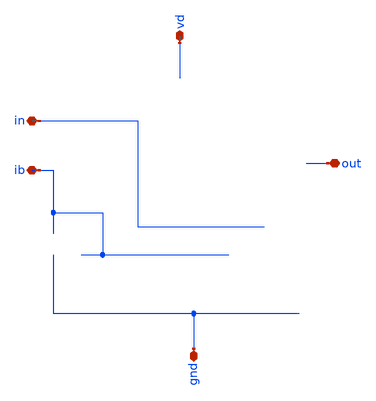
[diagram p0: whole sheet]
** sch_path: buffer/xschem/buffer-pex.sch
* Copyright 2020 Stefan Frederik Schippers
* Licensed under the Apache License, Version 2.0 (the "License");
* you may not use this file except in compliance with the License.
* You may obtain a copy of the License at
* https://www.apache.org/licenses/LICENSE-2.0
* Unless required by applicable law or agreed to in writing, software
* distributed under the License is distributed on an "AS IS" BASIS,
* WITHOUT WARRANTIES OR CONDITIONS OF ANY KIND, either express or implied.
* See the License for the specific language governing permissions and
* limitations under the License.
**.subckt buffer-pex vd ib out in gnd
*.iopin vd
*.iopin ib
*.iopin out
*.iopin in
*.iopin gnd
**** begin user architecture code


* NGSPICE file created from buffer.ext - technology: sky130A

*.subckt buffer vd ib out in gnd
X0 b.t2 b.t1 vd.t23 vd.t22 sky130_fd_pr__pfet_01v8 ad=0.145 pd=1.29 as=0.145 ps=1.29 w=1 l=1
X1 vd.t6 vd.t3 vd.t5 vd.t4 sky130_fd_pr__pfet_01v8 ad=0.29 pd=2.58 as=0 ps=0 w=1 l=1
X2 c out.t9 a gnd.t8 sky130_fd_pr__nfet_01v8 ad=0.248 pd=1.83 as=0.248 ps=1.83 w=1.5 l=0.15
X3 out.t5 d.t12 gnd.t19 gnd.t18 sky130_fd_pr__nfet_01v8 ad=0.725 pd=5.29 as=0.725 ps=5.29 w=5 l=1
X4 a a a vd.t39 sky130_fd_pr__pfet_01v8 ad=0.145 pd=1.29 as=1.16 ps=10.3 w=1 l=1
X5 d.t11 a vd.t38 vd.t37 sky130_fd_pr__pfet_01v8 ad=2.17 pd=15.3 as=2.17 ps=15.3 w=15 l=1
X6 d.t9 d.t8 d.t9 vd.t24 sky130_fd_pr__pfet_01v8 ad=2.17 pd=15.3 as=0 ps=0 w=15 l=1
X7 vd.t2 vd.t0 vd.t2 vd.t1 sky130_fd_pr__pfet_01v8 ad=0.145 pd=1.29 as=0 ps=0 w=1 l=1
X8 a a vd.t36 vd.t35 sky130_fd_pr__pfet_01v8 ad=0.145 pd=1.29 as=0.145 ps=1.29 w=1 l=1
X9 gnd.t22 d.t13 out.t8 gnd.t21 sky130_fd_pr__nfet_01v8 ad=0.725 pd=5.29 as=0.725 ps=5.29 w=5 l=1
X10 vd.t21 b.t16 out.t7 vd.t20 sky130_fd_pr__pfet_01v8 ad=2.17 pd=15.3 as=2.17 ps=15.3 w=15 l=1
X11 out.t4 out.t2 out.t3 vd.t40 sky130_fd_pr__pfet_01v8 ad=4.35 pd=30.6 as=0 ps=0 w=15 l=1
X12 d.t4 d.t3 gnd.t12 gnd.t11 sky130_fd_pr__nfet_01v8 ad=0.725 pd=5.29 as=0.725 ps=5.29 w=5 l=1
X13 a a vd.t34 vd.t33 sky130_fd_pr__pfet_01v8 ad=0.145 pd=1.29 as=0.145 ps=1.29 w=1 l=1
X14 b.t9 b.t7 b.t8 vd.t19 sky130_fd_pr__pfet_01v8 ad=0.29 pd=2.58 as=0 ps=0 w=1 l=1
X15 a a a gnd.t23 sky130_fd_pr__nfet_01v8 ad=0.465 pd=3.62 as=0.96 ps=7.28 w=1.5 l=0.15
X16 gnd.t7 gnd.t4 gnd.t6 gnd.t5 sky130_fd_pr__nfet_01v8 ad=1.45 pd=10.6 as=0 ps=0 w=5 l=1
X17 vd.t32 a a vd.t31 sky130_fd_pr__pfet_01v8 ad=0.145 pd=1.29 as=0.145 ps=1.29 w=1 l=1
X18 vd.t30 a a vd.t29 sky130_fd_pr__pfet_01v8 ad=0.145 pd=1.29 as=0.145 ps=1.29 w=1 l=1
X19 a a vd.t28 vd.t27 sky130_fd_pr__pfet_01v8 ad=0.145 pd=1.29 as=0.145 ps=1.29 w=1 l=1
X20 out.t10 d.t0 sky130_fd_pr__cap_mim_m3_1 l=15 w=30
X21 b.t6 b.t5 b.t6 gnd.t20 sky130_fd_pr__nfet_01v8 ad=0.248 pd=1.83 as=0 ps=0 w=1.5 l=0.15
X22 gnd.t10 ib.t0 ib.t1 gnd.t9 sky130_fd_pr__nfet_01v8 ad=0.145 pd=1.29 as=0.145 ps=1.29 w=1 l=1
X23 c ib.t5 gnd.t16 gnd.t15 sky130_fd_pr__nfet_01v8 ad=0.145 pd=1.29 as=0.145 ps=1.29 w=1 l=1
X24 ib.t4 ib.t2 ib.t3 gnd.t17 sky130_fd_pr__nfet_01v8 ad=0.29 pd=2.58 as=0 ps=0 w=1 l=1
X25 out.t6 b.t17 vd.t18 vd.t17 sky130_fd_pr__pfet_01v8 ad=2.17 pd=15.3 as=2.17 ps=15.3 w=15 l=1
X26 b.t15 b.t14 vd.t16 vd.t15 sky130_fd_pr__pfet_01v8 ad=0.145 pd=1.29 as=0.145 ps=1.29 w=1 l=1
X27 vd.t14 b.t10 b.t11 vd.t13 sky130_fd_pr__pfet_01v8 ad=0.145 pd=1.29 as=0.145 ps=1.29 w=1 l=1
X28 gnd.t14 d.t1 d.t2 gnd.t13 sky130_fd_pr__nfet_01v8 ad=0.725 pd=5.29 as=0.725 ps=5.29 w=5 l=1
X29 out.t1 out.t0 out.t1 vd.t7 sky130_fd_pr__pfet_01v8 ad=2.17 pd=15.3 as=0 ps=0 w=15 l=1
X30 vd.t12 b.t3 b.t4 vd.t11 sky130_fd_pr__pfet_01v8 ad=0.145 pd=1.29 as=0.145 ps=1.29 w=1 l=1
X31 b.t0 in.t0 c gnd.t0 sky130_fd_pr__nfet_01v8 ad=0.248 pd=1.83 as=0.248 ps=1.83 w=1.5 l=0.15
X32 c c c gnd.t24 sky130_fd_pr__nfet_01v8 ad=0.145 pd=1.29 as=1.08 ps=8.82 w=1 l=1
X33 vd.t26 a d.t10 vd.t25 sky130_fd_pr__pfet_01v8 ad=2.17 pd=15.3 as=2.17 ps=15.3 w=15 l=1
X34 d.t7 d.t5 d.t6 vd.t8 sky130_fd_pr__pfet_01v8 ad=4.35 pd=30.6 as=0 ps=0 w=15 l=1
X35 vd.t10 b.t12 b.t13 vd.t9 sky130_fd_pr__pfet_01v8 ad=0.145 pd=1.29 as=0.145 ps=1.29 w=1 l=1
X36 gnd.t3 gnd.t1 gnd.t3 gnd.t2 sky130_fd_pr__nfet_01v8 ad=0.725 pd=5.29 as=0 ps=0 w=5 l=1
R0 b.n6 b.t17 377.466
R1 b.n6 b.t16 376.93
R2 b.n16 b.t5 313.991
R3 b.t12 b.n6 41.3792
R4 b.n7 b.t12 40.2104
R5 b.n11 b.t9 28.6605
R6 b.n0 b.t11 28.5655
R7 b.n0 b.t8 28.5655
R8 b.n2 b.t13 28.5655
R9 b.n2 b.t2 28.5655
R10 b.n3 b.t4 28.5655
R11 b.n3 b.t15 28.5655
R12 b.n11 b.t7 26.2653
R13 b.n10 b.t10 26.2652
R14 b.n9 b.t14 26.2652
R15 b.n8 b.t3 26.2652
R16 b.n7 b.t1 26.2652
R17 b.n15 b.t0 13.2053
R18 b.n15 b.t6 6.63265
R19 b.n4 b.n2 1.62544
R20 b.n5 b.n4 1.44539
R21 b.n1 b.n10 0.825504
R22 b.n8 b.n7 0.718158
R23 b.n9 b.n8 0.718158
R24 b.n10 b.n9 0.718158
R25 b b.n16 0.594255
R26 b b.n14 0.562809
R27 b.n13 b.n12 0.188
R28 b.n4 b.n3 0.156686
R29 b.n12 b.n1 0.10675
R30 b.n13 b.n5 0.104667
R31 b.n16 b.n15 0.0678366
R32 b.n14 b.n0 0.0624088
R33 b.n1 b.n11 0.0623624
R34 b.n0 b.n13 0.0505
R35 vd.n49 vd.n48 647.907
R36 vd.n49 vd.n32 647.529
R37 vd.t1 vd.t9 331.216
R38 vd.t9 vd.t22 331.216
R39 vd.t15 vd.t11 331.216
R40 vd.t13 vd.t15 331.216
R41 vd.t19 vd.t13 331.216
R42 vd.t39 vd.t33 331.216
R43 vd.t33 vd.t31 331.216
R44 vd.t31 vd.t27 331.216
R45 vd.t35 vd.t29 331.216
R46 vd.t4 vd.t35 331.216
R47 vd.n36 vd.t39 228.514
R48 vd.n35 vd.t19 210.542
R49 vd.t24 vd.t37 70.1694
R50 vd.t25 vd.t8 70.1694
R51 vd.t17 vd.t7 70.0291
R52 vd.t40 vd.t20 70.0291
R53 vd.n45 vd.t24 68.5376
R54 vd.t8 vd.n39 63.6434
R55 vd.n29 vd.t40 63.5148
R56 vd.t7 vd.n23 62.9732
R57 vd.n14 vd.t0 39.5312
R58 vd.n4 vd.t3 39.5292
R59 vd.n36 vd.n35 38.514
R60 vd.n42 vd.t25 37.5327
R61 vd.n26 vd.t17 35.2862
R62 vd.t20 vd.n26 34.7434
R63 vd.t37 vd.n42 32.6372
R64 vd.n4 vd.t6 28.6459
R65 vd.n1 vd.t34 28.5655
R66 vd.n1 vd.t32 28.5655
R67 vd.n3 vd.t36 28.5655
R68 vd.n3 vd.t5 28.5655
R69 vd.n6 vd.t28 28.5655
R70 vd.n6 vd.t30 28.5655
R71 vd.n19 vd.t16 28.5655
R72 vd.n19 vd.t14 28.5655
R73 vd.n15 vd.t2 28.5655
R74 vd.n15 vd.t10 28.5655
R75 vd.n17 vd.t23 28.5655
R76 vd.n17 vd.t12 28.5655
R77 vd.n30 vd.n29 21.216
R78 vd.n31 vd.n30 16.7426
R79 vd.n46 vd.t4 16.3842
R80 vd.n46 vd.n45 16.211
R81 vd.n30 vd.t1 12.5482
R82 vd.n47 vd.n46 7.64222
R83 vd.n21 vd.n13 3.54402
R84 vd.n12 vd.n11 3.47391
R85 vd.n11 vd.t38 1.90483
R86 vd.n11 vd.t26 1.90483
R87 vd.n13 vd.t18 1.90483
R88 vd.n13 vd.t21 1.90483
R89 vd.n18 vd.n16 1.56925
R90 vd.n7 vd.n5 1.5417
R91 vd.n20 vd.n18 1.44593
R92 vd.n8 vd.n7 1.38331
R93 vd.n16 vd.n14 0.686006
R94 vd.n50 vd.n21 0.503104
R95 vd vd.n12 0.497524
R96 vd.n21 vd.n20 0.424134
R97 vd.n12 vd.n10 0.313286
R98 vd.n18 vd.n17 0.157684
R99 vd.n7 vd.n6 0.156686
R100 vd.n5 vd.n4 0.0791768
R101 vd.n5 vd.n3 0.0493677
R102 vd.n9 vd.n8 0.0489375
R103 vd.n16 vd.n15 0.0461626
R104 vd vd.n50 0.0239375
R105 vd.n2 vd.n1 0.0200317
R106 vd.n10 vd.n0 0.01975
R107 vd.n20 vd.n19 0.0148061
R108 vd.n9 vd.n2 0.0083125
R109 vd.n25 vd.n24 0.00431884
R110 vd.n26 vd.n25 0.00431884
R111 vd.n41 vd.n40 0.00425193
R112 vd.n42 vd.n41 0.00425193
R113 vd.n48 vd.n47 0.00389051
R114 vd.n32 vd.n31 0.00389051
R115 vd.n44 vd.n43 0.0021559
R116 vd.n45 vd.n44 0.0021559
R117 vd.n28 vd.n27 0.00213065
R118 vd.n29 vd.n28 0.00213065
R119 vd.n39 vd.n38 0.00181202
R120 vd.n23 vd.n22 0.00181202
R121 vd.n34 vd.n33 0.0017783
R122 vd.n35 vd.n34 0.0017783
R123 vd.n10 vd.n9 0.00100557
R124 vd.n49 vd.n37 0.000827345
R125 vd.n37 vd.n36 0.000827345
R126 vd.n50 vd.n49 0.000504092
R127 out.n4 out.t2 377.192
R128 out.n1 out.t0 377.175
R129 out.n6 out.t9 317.7
R130 out.n9 out.t4 5.53268
R131 out.n7 out.t8 3.4805
R132 out.n7 out.t5 3.4805
R133 out.n5 out.n4 2.02858
R134 out.n2 out.n1 2.00736
R135 out.n3 out.t7 1.90483
R136 out.n3 out.t3 1.90483
R137 out.n0 out.t1 1.90483
R138 out.n0 out.t6 1.90483
R139 out.n6 out.t10 1.8318
R140 out.n8 out.n7 1.58206
R141 out.n10 out.n9 0.80675
R142 out out.n10 0.783312
R143 out.n9 out.n8 0.770812
R144 out.n10 out.n2 0.182565
R145 out.n9 out.n5 0.182565
R146 out.n5 out.n3 0.00195207
R147 out.n2 out.n0 0.00195207
R148 out.n8 out.n6 0.000558569
R149 gnd.n15 gnd.n12 560.566
R150 gnd.n33 gnd.n30 547.013
R151 gnd.t13 gnd.t11 412.351
R152 gnd.t15 gnd.t24 412.351
R153 gnd.n13 gnd.t2 348.421
R154 gnd.n36 gnd.n28 256.471
R155 gnd.n23 gnd.n22 242.918
R156 gnd.n16 gnd.t13 217.363
R157 gnd.n34 gnd.t9 214.167
R158 gnd.n34 gnd.t15 198.185
R159 gnd.n16 gnd.t18 194.988
R160 gnd.t8 gnd.t23 153.434
R161 gnd.n23 gnd.n15 147.294
R162 gnd.n36 gnd.n33 133.742
R163 gnd.n26 gnd.t8 107.084
R164 gnd.t5 gnd.t20 107.084
R165 gnd.n6 gnd.t4 65.675
R166 gnd.n0 gnd.t1 65.5414
R167 gnd.n13 gnd.t21 63.9308
R168 gnd.n20 gnd.t5 35.1621
R169 gnd.n25 gnd.t16 17.4005
R170 gnd.n25 gnd.t10 17.4005
R171 gnd.n31 gnd.t17 12.7866
R172 gnd.n20 gnd.t0 11.1883
R173 gnd.n6 gnd.t7 6.44128
R174 gnd.n38 gnd.n24 6.30056
R175 gnd.n38 gnd.n37 5.41306
R176 gnd.n3 gnd.t19 3.4805
R177 gnd.n3 gnd.t14 3.4805
R178 gnd.n1 gnd.t3 3.4805
R179 gnd.n1 gnd.t22 3.4805
R180 gnd.n7 gnd.t12 3.4805
R181 gnd.n7 gnd.t6 3.4805
R182 gnd.n2 gnd.n0 3.21916
R183 gnd.n8 gnd.n6 2.95318
R184 gnd gnd.n38 1.74425
R185 gnd.n37 gnd.n25 1.41862
R186 gnd.n5 gnd.n2 0.6455
R187 gnd.n9 gnd.n8 0.62925
R188 gnd.n24 gnd.n10 0.425505
R189 gnd.n10 gnd.n9 0.063
R190 gnd.n33 gnd.n32 0.0431634
R191 gnd.n32 gnd.n31 0.0431634
R192 gnd.n15 gnd.n14 0.0388129
R193 gnd.n14 gnd.n13 0.0388129
R194 gnd.n28 gnd.n27 0.0215341
R195 gnd.n27 gnd.n26 0.0215341
R196 gnd.n9 gnd.n5 0.01675
R197 gnd.n22 gnd.n21 0.00984699
R198 gnd.n21 gnd.n20 0.00984699
R199 gnd.n30 gnd.n29 0.007537
R200 gnd.n12 gnd.n11 0.007537
R201 gnd.n36 gnd.n35 0.00701261
R202 gnd.n35 gnd.n34 0.00701261
R203 gnd.n23 gnd.n17 0.00701261
R204 gnd.n17 gnd.n16 0.00701261
R205 gnd.n19 gnd.n18 0.00517349
R206 gnd.n20 gnd.n19 0.00517349
R207 gnd.n5 gnd.n4 0.00371923
R208 gnd.n2 gnd.n1 0.00294771
R209 gnd.n8 gnd.n7 0.00294771
R210 gnd.n4 gnd.n3 0.00217489
R211 gnd.n37 gnd.n36 0.00148887
R212 gnd.n24 gnd.n23 0.000506305
R213 d.n9 d.t5 377.216
R214 d.n8 d.t8 377.163
R215 d.n2 d.t13 134.298
R216 d.n4 d.t3 133.787
R217 d.n3 d.t1 133.761
R218 d.n2 d.t12 133.761
R219 d.n0 d.t7 5.55126
R220 d.n6 d.t2 3.4805
R221 d.n6 d.t4 3.4805
R222 d d.n7 3.10062
R223 d.n0 d.n9 2.02586
R224 d.n1 d.n8 1.99422
R225 d.n5 d.t0 1.92689
R226 d.n1 d.t11 1.90534
R227 d.n0 d.t10 1.90483
R228 d.n0 d.t6 1.90483
R229 d.n1 d.t9 1.89094
R230 d d.n1 0.77675
R231 d.n1 d.n0 0.647901
R232 d.n3 d.n2 0.538
R233 d.n4 d.n3 0.394346
R234 d.n7 d.n6 0.151643
R235 d.n5 d.n4 0.0558728
R236 d.n7 d.n5 0.0333947
R237 ib.n0 ib.t5 38.0465
R238 ib.n0 ib.t0 37.3602
R239 ib.n4 ib.t2 18.7496
R240 ib.n4 ib.t4 17.4934
R241 ib.n1 ib.t1 17.4005
R242 ib.n1 ib.t3 17.4005
R243 ib ib.n8 5.82556
R244 ib.n3 ib.n2 1.98477
R245 ib.n8 ib.n0 0.247263
R246 ib.n5 ib.n4 0.102062
R247 ib.n8 ib.n7 0.059593
R248 ib.n7 ib.n6 0.0239375
R249 ib.n6 ib.n3 0.0166802
R250 ib.n6 ib.n5 0.003625
R251 ib.n3 ib.n1 0.00322924
R252 in in.t0 325.817
C0 a c 0.199f
C1 d ib 0.576f
C2 in c 0.416f
C3 a b 0.239f
C4 b in 0.112f
C5 a vd 5.21f
C6 a out 0.0945f
C7 vd in 0.376f
C8 b c 0.16f
C9 in out 0.054f
C10 vd c 0.00332f
C11 a ib 0.00973f
C12 a d 1.29f
C13 out c 0.0405f
C14 in ib 0.573f
C15 b vd 6.07f
C16 d in 0.668f
C17 b out 1.93f
C18 ib c 0.185f
C19 d c 0.0518f
C20 vd out 4.7f
C21 b d 0.0519f
C22 vd ib 0.0124f
C23 vd d 3.9f
C24 out ib 0.0617f
C25 a in 0.227f
C26 d out 40.7f
*.ends



**** end user architecture code
**.ends
.end
